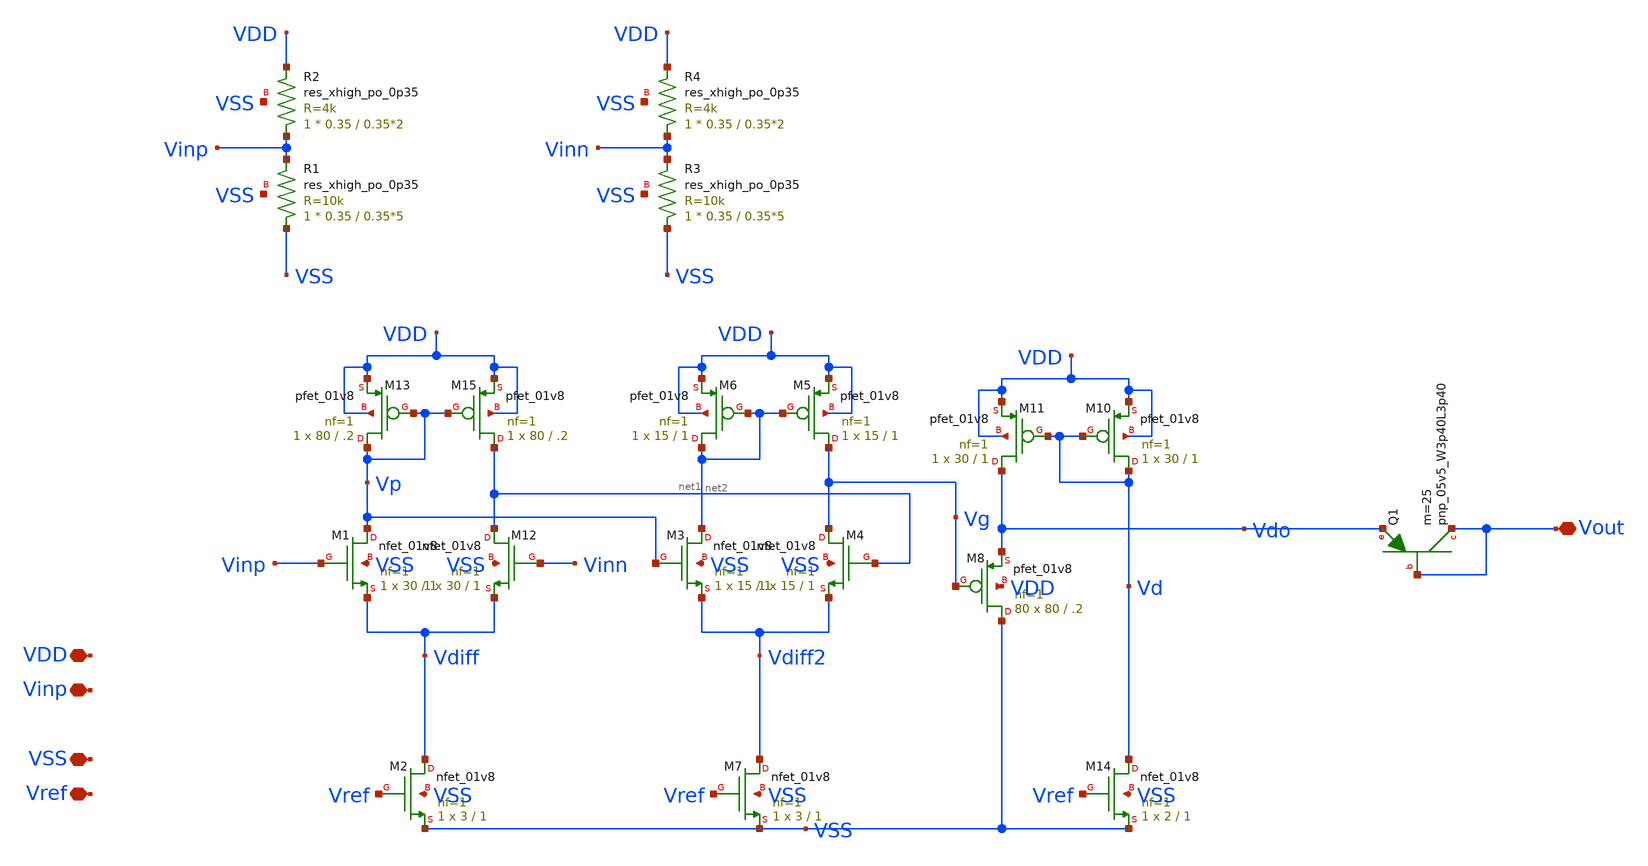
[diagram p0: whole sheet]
** sch_path: Project/xschem/demod.sch
**.subckt demod Vref VSS Vinp VDD Vout
*.iopin Vref
*.iopin VSS
*.iopin Vinp
*.iopin VDD
*.iopin Vout
XM1 Vp Vinp Vdiff VSS sky130_fd_pr__nfet_01v8 L=1 W=30 nf=1 ad='int((nf+1)/2) * W/nf * 0.29' as='int((nf+2)/2) * W/nf * 0.29'
+ pd='2*int((nf+1)/2) * (W/nf + 0.29)' ps='2*int((nf+2)/2) * (W/nf + 0.29)' nrd='0.29 / W' nrs='0.29 / W'
+ sa=0 sb=0 sd=0 mult=1 m=1
XM12 net1 Vinn Vdiff VSS sky130_fd_pr__nfet_01v8 L=1 W=30 nf=1 ad='int((nf+1)/2) * W/nf * 0.29' as='int((nf+2)/2) * W/nf * 0.29'
+ pd='2*int((nf+1)/2) * (W/nf + 0.29)' ps='2*int((nf+2)/2) * (W/nf + 0.29)' nrd='0.29 / W' nrs='0.29 / W'
+ sa=0 sb=0 sd=0 mult=1 m=1
XM15 net1 Vp VDD VDD sky130_fd_pr__pfet_01v8 L=.2 W=80 nf=1 ad='int((nf+1)/2) * W/nf * 0.29' as='int((nf+2)/2) * W/nf * 0.29'
+ pd='2*int((nf+1)/2) * (W/nf + 0.29)' ps='2*int((nf+2)/2) * (W/nf + 0.29)' nrd='0.29 / W' nrs='0.29 / W'
+ sa=0 sb=0 sd=0 mult=1 m=1
XM13 Vp Vp VDD VDD sky130_fd_pr__pfet_01v8 L=.2 W=80 nf=1 ad='int((nf+1)/2) * W/nf * 0.29' as='int((nf+2)/2) * W/nf * 0.29'
+ pd='2*int((nf+1)/2) * (W/nf + 0.29)' ps='2*int((nf+2)/2) * (W/nf + 0.29)' nrd='0.29 / W' nrs='0.29 / W'
+ sa=0 sb=0 sd=0 mult=1 m=1
XM2 Vdiff Vref VSS VSS sky130_fd_pr__nfet_01v8 L=1 W=3 nf=1 ad='int((nf+1)/2) * W/nf * 0.29' as='int((nf+2)/2) * W/nf * 0.29'
+ pd='2*int((nf+1)/2) * (W/nf + 0.29)' ps='2*int((nf+2)/2) * (W/nf + 0.29)' nrd='0.29 / W' nrs='0.29 / W'
+ sa=0 sb=0 sd=0 mult=1 m=1
XM10 Vd Vd VDD VDD sky130_fd_pr__pfet_01v8 L=1 W=30 nf=1 ad='int((nf+1)/2) * W/nf * 0.29' as='int((nf+2)/2) * W/nf * 0.29'
+ pd='2*int((nf+1)/2) * (W/nf + 0.29)' ps='2*int((nf+2)/2) * (W/nf + 0.29)' nrd='0.29 / W' nrs='0.29 / W'
+ sa=0 sb=0 sd=0 mult=1 m=1
XM11 Vdo Vd VDD VDD sky130_fd_pr__pfet_01v8 L=1 W=30 nf=1 ad='int((nf+1)/2) * W/nf * 0.29' as='int((nf+2)/2) * W/nf * 0.29'
+ pd='2*int((nf+1)/2) * (W/nf + 0.29)' ps='2*int((nf+2)/2) * (W/nf + 0.29)' nrd='0.29 / W' nrs='0.29 / W'
+ sa=0 sb=0 sd=0 mult=1 m=1
XM14 Vd Vref VSS VSS sky130_fd_pr__nfet_01v8 L=1 W=2 nf=1 ad='int((nf+1)/2) * W/nf * 0.29' as='int((nf+2)/2) * W/nf * 0.29'
+ pd='2*int((nf+1)/2) * (W/nf + 0.29)' ps='2*int((nf+2)/2) * (W/nf + 0.29)' nrd='0.29 / W' nrs='0.29 / W'
+ sa=0 sb=0 sd=0 mult=1 m=1
XM8 VSS Vg Vdo VDD sky130_fd_pr__pfet_01v8 L=.2 W=80 nf=1 ad='int((nf+1)/2) * W/nf * 0.29' as='int((nf+2)/2) * W/nf * 0.29'
+ pd='2*int((nf+1)/2) * (W/nf + 0.29)' ps='2*int((nf+2)/2) * (W/nf + 0.29)' nrd='0.29 / W' nrs='0.29 / W'
+ sa=0 sb=0 sd=0 mult=80 m=80
XQ1 Vout Vout Vdo sky130_fd_pr__pnp_05v5_W3p40L3p40 m=25
XR1 VSS Vinp VSS sky130_fd_pr__res_xhigh_po_0p35 L=0.35*5 mult=1 m=1
XR2 Vinp VDD VSS sky130_fd_pr__res_xhigh_po_0p35 L=0.35*2 mult=1 m=1
XR3 VSS Vinn VSS sky130_fd_pr__res_xhigh_po_0p35 L=0.35*5 mult=1 m=1
XR4 Vinn VDD VSS sky130_fd_pr__res_xhigh_po_0p35 L=0.35*2 mult=1 m=1
XM3 net2 Vp Vdiff2 VSS sky130_fd_pr__nfet_01v8 L=1 W=15 nf=1 ad='int((nf+1)/2) * W/nf * 0.29' as='int((nf+2)/2) * W/nf * 0.29'
+ pd='2*int((nf+1)/2) * (W/nf + 0.29)' ps='2*int((nf+2)/2) * (W/nf + 0.29)' nrd='0.29 / W' nrs='0.29 / W'
+ sa=0 sb=0 sd=0 mult=1 m=1
XM4 Vg net1 Vdiff2 VSS sky130_fd_pr__nfet_01v8 L=1 W=15 nf=1 ad='int((nf+1)/2) * W/nf * 0.29' as='int((nf+2)/2) * W/nf * 0.29'
+ pd='2*int((nf+1)/2) * (W/nf + 0.29)' ps='2*int((nf+2)/2) * (W/nf + 0.29)' nrd='0.29 / W' nrs='0.29 / W'
+ sa=0 sb=0 sd=0 mult=1 m=1
XM5 Vg net2 VDD VDD sky130_fd_pr__pfet_01v8 L=1 W=15 nf=1 ad='int((nf+1)/2) * W/nf * 0.29' as='int((nf+2)/2) * W/nf * 0.29'
+ pd='2*int((nf+1)/2) * (W/nf + 0.29)' ps='2*int((nf+2)/2) * (W/nf + 0.29)' nrd='0.29 / W' nrs='0.29 / W'
+ sa=0 sb=0 sd=0 mult=1 m=1
XM6 net2 net2 VDD VDD sky130_fd_pr__pfet_01v8 L=1 W=15 nf=1 ad='int((nf+1)/2) * W/nf * 0.29' as='int((nf+2)/2) * W/nf * 0.29'
+ pd='2*int((nf+1)/2) * (W/nf + 0.29)' ps='2*int((nf+2)/2) * (W/nf + 0.29)' nrd='0.29 / W' nrs='0.29 / W'
+ sa=0 sb=0 sd=0 mult=1 m=1
XM7 Vdiff2 Vref VSS VSS sky130_fd_pr__nfet_01v8 L=1 W=3 nf=1 ad='int((nf+1)/2) * W/nf * 0.29' as='int((nf+2)/2) * W/nf * 0.29'
+ pd='2*int((nf+1)/2) * (W/nf + 0.29)' ps='2*int((nf+2)/2) * (W/nf + 0.29)' nrd='0.29 / W' nrs='0.29 / W'
+ sa=0 sb=0 sd=0 mult=1 m=1
**.ends
.end
